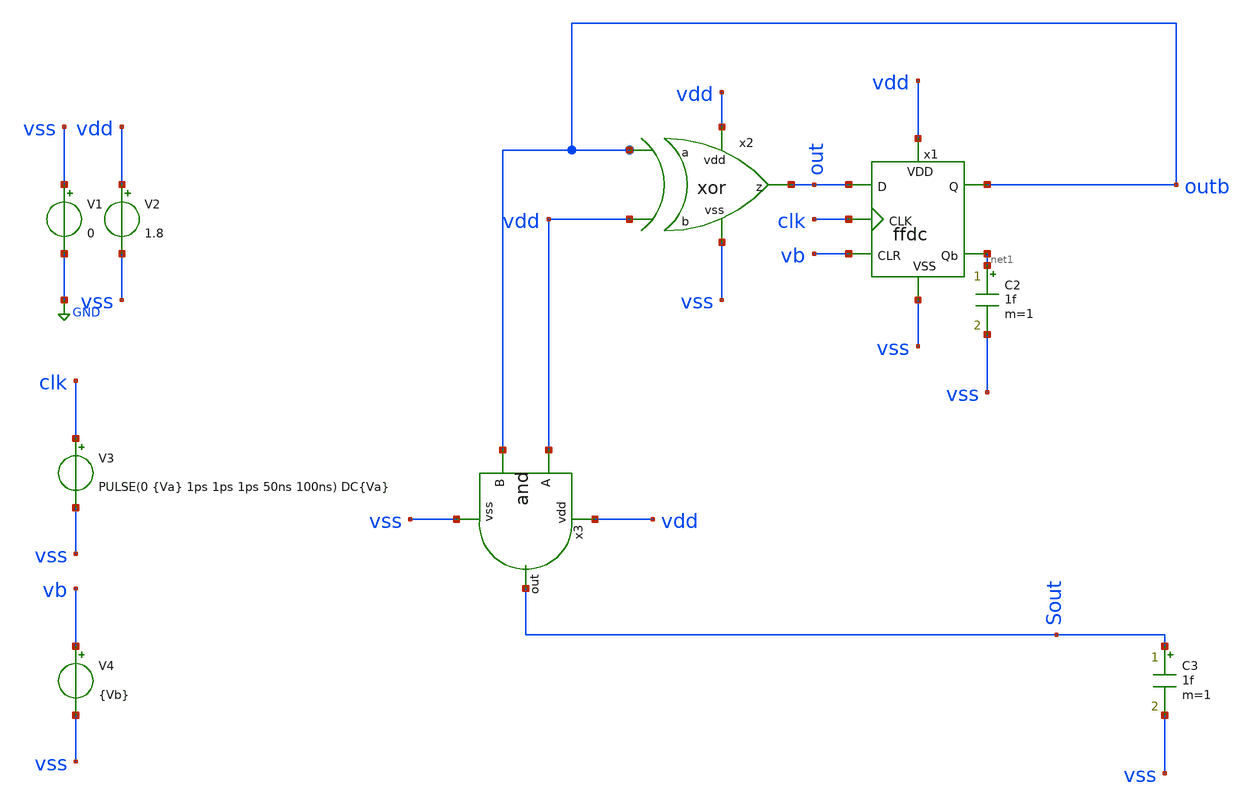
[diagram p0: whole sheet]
** sch_path: track_vlsi/ledesma/sch/tb_bitc.sch
**.subckt tb_bitc
V1 vss GND 0
V2 vdd vss 1.8
V3 clk vss PULSE(0 {Va} 1ps 1ps 1ps 50ns 100ns) DC{Va}
V4 vb vss {Vb}
x2 vdd outb vdd out vss xor
x3 vdd vdd outb Sout vss and
C2 net1 vss 1f m=1
C3 Sout vss 1f m=1
x1 vdd vss outb out clk vb net1 ffdc
**** begin user architecture code



* Parametros del circuito
.param Va=1.8
.param Vb=0
.options TEMP = 27.0

* Include
.lib /home/eamta/skywater/skywater-pdk/libraries/sky130_fd_pr_ngspice/latest/models/corners/sky130.lib TT

*simulation
.control
  tran 1n 300ns
  setplot tran1
  plot v(outb) v(clk)+1.8
  write tb_and_tran.raw


.endc
.end


**** end user architecture code
**.ends
.GLOBAL GND
.end
